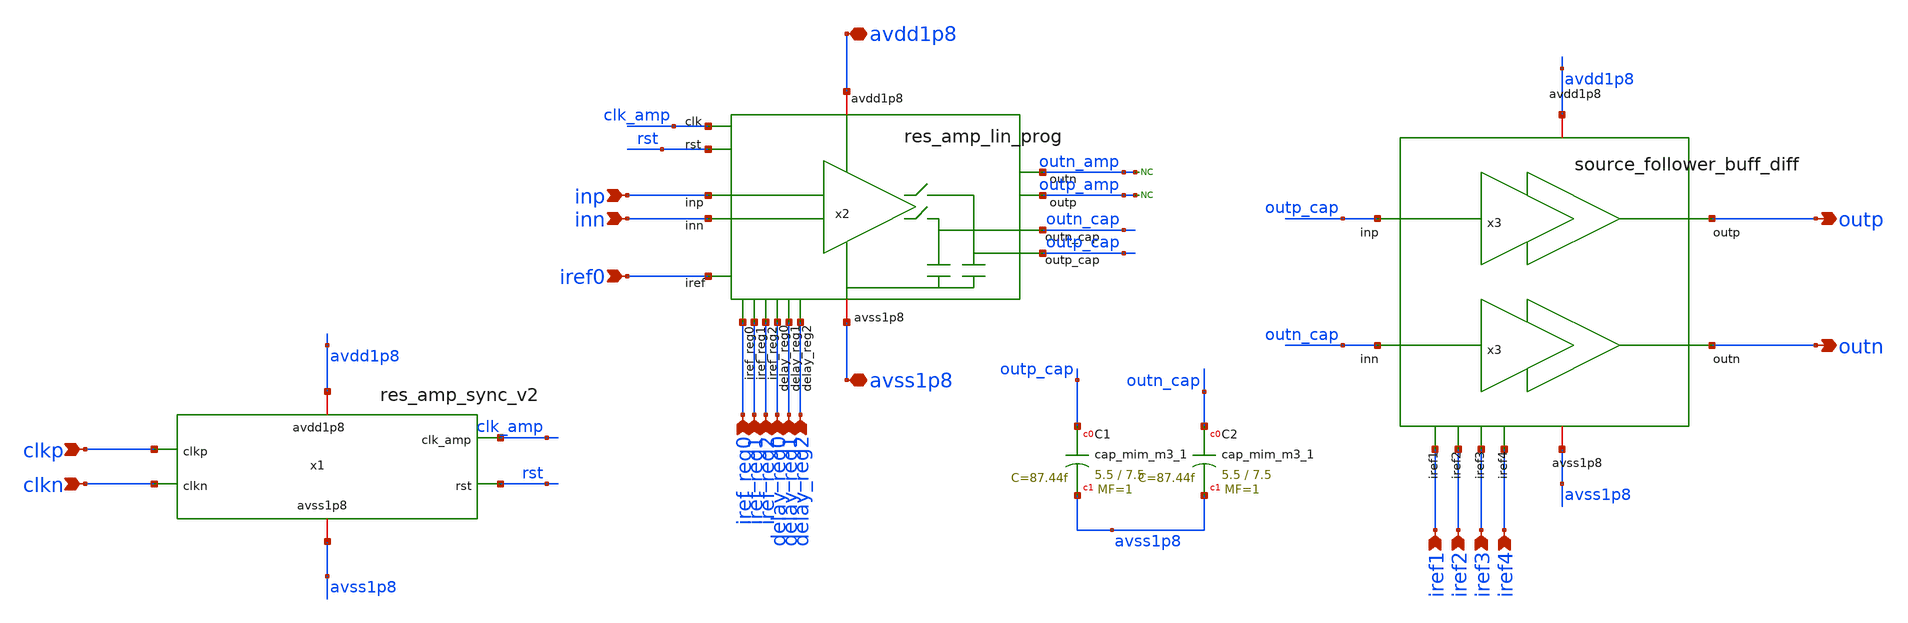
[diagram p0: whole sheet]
** sch_path: xschem/res_amp_top.sch
**.subckt res_amp_top inp inn clkp clkn avdd1p8 avss1p8 iref0 iref1 iref2 iref3 iref4 outn outp
*+ iref_reg0 iref_reg1 iref_reg2 delay_reg0 delay_reg1 delay_reg2
*.ipin inp
*.ipin inn
*.ipin clkp
*.ipin clkn
*.iopin avdd1p8
*.iopin avss1p8
*.ipin iref0
*.ipin iref1
*.ipin iref2
*.ipin iref3
*.ipin iref4
*.opin outn
*.opin outp
*.ipin iref_reg0
*.ipin iref_reg1
*.ipin iref_reg2
*.ipin delay_reg0
*.ipin delay_reg1
*.ipin delay_reg2
x2 avdd1p8 rst inp inn outp_amp outn_amp avss1p8 outp_cap outn_cap clk_amp iref_reg0 iref_reg1
+ iref_reg2 delay_reg0 delay_reg2 delay_reg1 iref0 res_amp_lin_prog
x1 avdd1p8 clkp clkn avss1p8 clk_amp rst res_amp_sync_v2
x3 avdd1p8 iref1 outp_cap outp avss1p8 outn_cap outn iref2 iref3 iref4 source_follower_buff_diff
* noconn outn_amp
* noconn outp_amp
XC1 outp_cap avss1p8 sky130_fd_pr__cap_mim_m3_1 W=5.5 L=7.5 MF=1 m=1
XC2 outn_cap avss1p8 sky130_fd_pr__cap_mim_m3_1 W=5.5 L=7.5 MF=1 m=1
**.ends
.end
